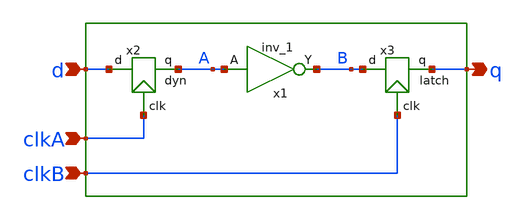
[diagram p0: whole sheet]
** sch_path: src/xe/test_cases/dyn_latch.sch
**.subckt dyn_latch d clkA q clkB
*.ipin d
*.ipin clkA
*.opin q
*.ipin clkB
x1 A vss vss vcc vcc B sky130_fd_sc_hd__inv_1
x3 clkB q B latch
x2 clkA A d dyn
**.ends

* expanding   symbol:  yxt/latch.sym # of pins=3
** sym_path: src/xe/test_cases/latch.sym
** sch_path: src/xe/test_cases/latch.sch
.subckt latch clk q d  vcc=vcc vss=vss
*.ipin clk
*.ipin d
*.opin q
x1 d vss vss vcc vcc db sky130_fd_sc_hd__inv_1
x2 clkb db z clk vcc vss tgate
x3 z vss vss vcc vcc q sky130_fd_sc_hd__inv_1
x6 clk vss vss vcc vcc clkb sky130_fd_sc_hd__inv_1
x4 z vss vss vcc vcc fb sky130_fd_sc_hd__inv_1
x5 fb vss vss vcc vcc z sky130_fd_sc_hd__inv_1
.ends


* expanding   symbol:  yxt/dyn.sym # of pins=3
** sym_path: src/xe/test_cases/dyn.sym
** sch_path: src/xe/test_cases/dyn.sch
.subckt dyn clk q d
*.ipin clk
*.opin q
*.ipin d
x1 z vss vss vcc vcc q sky130_fd_sc_hd__inv_1
XM1 z d net1 vss sky130_fd_pr__nfet_01v8 L=0.15 W=1 nf=1 ad='int((nf+1)/2) * W/nf * 0.29' as='int((nf+2)/2) * W/nf * 0.29'
+ pd='2*int((nf+1)/2) * (W/nf + 0.29)' ps='2*int((nf+2)/2) * (W/nf + 0.29)' nrd='0.29 / W' nrs='0.29 / W'
+ sa=0 sb=0 sd=0 mult=1 m=1
XM2 z q vcc vcc sky130_fd_pr__pfet_01v8 L=0.15 W=1 nf=1 ad='int((nf+1)/2) * W/nf * 0.29' as='int((nf+2)/2) * W/nf * 0.29'
+ pd='2*int((nf+1)/2) * (W/nf + 0.29)' ps='2*int((nf+2)/2) * (W/nf + 0.29)' nrd='0.29 / W' nrs='0.29 / W'
+ sa=0 sb=0 sd=0 mult=1 m=1
XM3 z clk vcc vcc sky130_fd_pr__pfet_01v8 L=0.15 W=1 nf=1 ad='int((nf+1)/2) * W/nf * 0.29' as='int((nf+2)/2) * W/nf * 0.29'
+ pd='2*int((nf+1)/2) * (W/nf + 0.29)' ps='2*int((nf+2)/2) * (W/nf + 0.29)' nrd='0.29 / W' nrs='0.29 / W'
+ sa=0 sb=0 sd=0 mult=1 m=1
XM4 net1 clk vss vss sky130_fd_pr__nfet_01v8 L=0.15 W=1 nf=1 ad='int((nf+1)/2) * W/nf * 0.29' as='int((nf+2)/2) * W/nf * 0.29'
+ pd='2*int((nf+1)/2) * (W/nf + 0.29)' ps='2*int((nf+2)/2) * (W/nf + 0.29)' nrd='0.29 / W' nrs='0.29 / W'
+ sa=0 sb=0 sd=0 mult=1 m=1
.ends


* expanding   symbol:  yxt/tgate.sym # of pins=4
** sym_path: src/xe/test_cases/tgate.sym
** sch_path: src/xe/test_cases/tgate.sch
.subckt tgate gp s d gn vcc vss
*.ipin s
*.ipin gp
*.ipin gn
*.opin d
XMpc d gp s vss sky130_fd_pr__pfet_01v8 L=0.15 W=1 nf=1 ad='int((nf+1)/2) * W/nf * 0.29' as='int((nf+2)/2) * W/nf * 0.29'
+ pd='2*int((nf+1)/2) * (W/nf + 0.29)' ps='2*int((nf+2)/2) * (W/nf + 0.29)' nrd='0.29 / W' nrs='0.29 / W'
+ sa=0 sb=0 sd=0 mult=7 m=7
XM15 s gn d vcc sky130_fd_pr__nfet_01v8 L=0.15 W=1 nf=1 ad='int((nf+1)/2) * W/nf * 0.29' as='int((nf+2)/2) * W/nf * 0.29'
+ pd='2*int((nf+1)/2) * (W/nf + 0.29)' ps='2*int((nf+2)/2) * (W/nf + 0.29)' nrd='0.29 / W' nrs='0.29 / W'
+ sa=0 sb=0 sd=0 mult=1 m=1
.ends

.end
